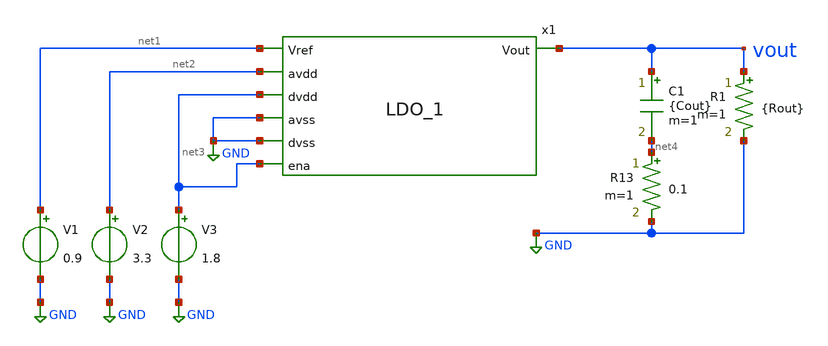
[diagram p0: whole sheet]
** sch_path: cace/test_temp.sch
**.subckt test_temp
V1 net1 GND 0.9
V2 net2 GND 3.3
V3 net3 GND 1.8
C1 vout net4 {Cout} m=1
R13 net4 GND 0.1 m=1
R1 vout GND {Rout} m=1
x1 net1 net2 net3 GND vout GND net3 LDO_1
**** begin user architecture code



.lib /home/dcdc/xschem-src/open_pdks/sky130/sky130A/libs.tech/ngspice/sky130.lib.spice tt

.param Cout = 2.2u
.param Rout = 22.5k
.save all
.option savecurrents

.param TEMGAUSS = agauss(-40, 85, 1)
.option temp = 'TEMGAUSS'

.control
	option seed = 9
	let run = 0
	dowhile run <=100
		save  all
		tran 100u 100000u uic
		remzerovec
		write LDO_v1_temp.raw
		set appendwrite
		reset
		let run = run + 20
		plot V(vout)
	end




.endc

.saveall



**** end user architecture code
**.ends

* expanding   symbol:
*+  /home/dcdc/xschem-src/Work1/chipalooza2024/sky130_deser_ip_lowpowerLDO/xschem/LDO_1.sym # of pins=7
** sym_path: xschem/LDO_1.sym
** sch_path: xschem/LDO_1.sch
.subckt LDO_1 Vref avdd dvdd avss Vout dvss ena
*.ipin avdd
*.ipin dvss
*.ipin dvdd
*.ipin avss
*.ipin ena
*.ipin Vref
*.opin Vout
XM1 vout Vout_fb1 avdd avdd sky130_fd_pr__pfet_01v8_hvt L=0.3 W=1 nf=1 ad='int((nf+1)/2) * W/nf * 0.29'
+ as='int((nf+2)/2) * W/nf * 0.29' pd='2*int((nf+1)/2) * (W/nf + 0.29)' ps='2*int((nf+2)/2) * (W/nf + 0.29)'
+ nrd='0.29 / W' nrs='0.29 / W' sa=0 sb=0 sd=0 mult=1 m=1
R4 vout Vfed 100k m=1
R5 Vfed avss 100k m=1
XM21 Vout_fb4 net2 avss GND sky130_fd_pr__nfet_01v8_lvt L=0.15 W=12 nf=1 ad='int((nf+1)/2) * W/nf * 0.29'
+ as='int((nf+2)/2) * W/nf * 0.29' pd='2*int((nf+1)/2) * (W/nf + 0.29)' ps='2*int((nf+2)/2) * (W/nf + 0.29)'
+ nrd='0.29 / W' nrs='0.29 / W' sa=0 sb=0 sd=0 mult=1 m=1
XM22 net2 net2 avss GND sky130_fd_pr__nfet_01v8_lvt L=0.15 W=12 nf=1 ad='int((nf+1)/2) * W/nf * 0.29'
+ as='int((nf+2)/2) * W/nf * 0.29' pd='2*int((nf+1)/2) * (W/nf + 0.29)' ps='2*int((nf+2)/2) * (W/nf + 0.29)'
+ nrd='0.29 / W' nrs='0.29 / W' sa=0 sb=0 sd=0 mult=1 m=1
XM23 Vout_fb1 Vout_fb4 avss avss sky130_fd_pr__nfet_01v8_lvt L=0.15 W=18 nf=1 ad='int((nf+1)/2) * W/nf * 0.29'
+ as='int((nf+2)/2) * W/nf * 0.29' pd='2*int((nf+1)/2) * (W/nf + 0.29)' ps='2*int((nf+2)/2) * (W/nf + 0.29)'
+ nrd='0.29 / W' nrs='0.29 / W' sa=0 sb=0 sd=0 mult=1 m=1
XM2 Vout_fb1 net4 avdd avdd sky130_fd_pr__pfet_01v8_lvt L=1 W=1 nf=1 ad='int((nf+1)/2) * W/nf * 0.29'
+ as='int((nf+2)/2) * W/nf * 0.29' pd='2*int((nf+1)/2) * (W/nf + 0.29)' ps='2*int((nf+2)/2) * (W/nf + 0.29)'
+ nrd='0.29 / W' nrs='0.29 / W' sa=0 sb=0 sd=0 mult=1 m=1
XM3 net2 Vref net1 avdd sky130_fd_pr__pfet_01v8_lvt L=0.35 W=10 nf=1 ad='int((nf+1)/2) * W/nf * 0.29'
+ as='int((nf+2)/2) * W/nf * 0.29' pd='2*int((nf+1)/2) * (W/nf + 0.29)' ps='2*int((nf+2)/2) * (W/nf + 0.29)'
+ nrd='0.29 / W' nrs='0.29 / W' sa=0 sb=0 sd=0 mult=1 m=1
XM4 Vout_fb4 Vfed net1 avdd sky130_fd_pr__pfet_01v8_lvt L=0.35 W=10 nf=1 ad='int((nf+1)/2) * W/nf * 0.29'
+ as='int((nf+2)/2) * W/nf * 0.29' pd='2*int((nf+1)/2) * (W/nf + 0.29)' ps='2*int((nf+2)/2) * (W/nf + 0.29)'
+ nrd='0.29 / W' nrs='0.29 / W' sa=0 sb=0 sd=0 mult=1 m=1
XM5 net1 net4 avdd avdd sky130_fd_pr__pfet_01v8_lvt L=1 W=1 nf=1 ad='int((nf+1)/2) * W/nf * 0.29' as='int((nf+2)/2) * W/nf * 0.29'
+ pd='2*int((nf+1)/2) * (W/nf + 0.29)' ps='2*int((nf+2)/2) * (W/nf + 0.29)' nrd='0.29 / W' nrs='0.29 / W'
+ sa=0 sb=0 sd=0 mult=1 m=1
XM6 net4 net4 avdd avdd sky130_fd_pr__pfet_01v8_lvt L=0.35 W=1 nf=1 ad='int((nf+1)/2) * W/nf * 0.29'
+ as='int((nf+2)/2) * W/nf * 0.29' pd='2*int((nf+1)/2) * (W/nf + 0.29)' ps='2*int((nf+2)/2) * (W/nf + 0.29)'
+ nrd='0.29 / W' nrs='0.29 / W' sa=0 sb=0 sd=0 mult=1 m=1
XR7 avss net4 avdd sky130_fd_pr__res_xhigh_po_5p73 L=5.73*10 mult=1 m=1
XC2 Vout_fb4 net3 sky130_fd_pr__cap_mim_m3_2 W=10 L=30 MF=1 m=1
R8 net3 Vout_fb1 sky130_fd_pr__res_generic_l1 W=1 L=19 m=1
.ends

.GLOBAL GND
.end
